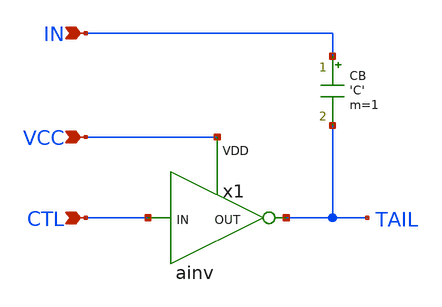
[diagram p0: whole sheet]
** sch_path: demo/cosim/test_new/vacask_cosim_hier/final_folder/ccap.sch
**.subckt ccap IN VCC CTL
*.ipin IN
*.ipin VCC
*.ipin CTL
CB IN TAIL 'C' m=1
x1 CTL TAIL VCC ainv
**.ends
.end
